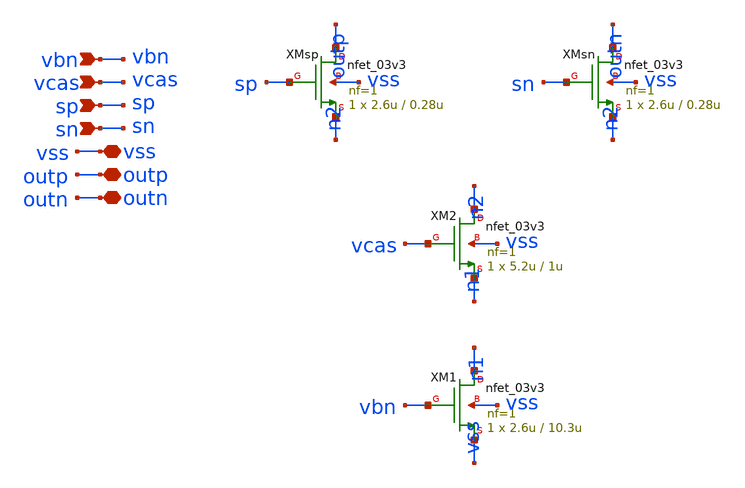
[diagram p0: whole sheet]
** sch_path: design/analog/unit_cell.sch
**.subckt unit_cell vbn vcas sp sn vss outp outn
*.ipin vbn
*.ipin vcas
*.ipin sp
*.ipin sn
*.iopin vss
*.iopin outp
*.iopin outn
XM1 n1 vbn vss vss nfet_03v3 L=10.3u W=2.6u nf=1 ad='int((nf+1)/2) * W/nf * 0.18u' as='int((nf+2)/2) * W/nf * 0.18u'
+ pd='2*int((nf+1)/2) * (W/nf + 0.18u)' ps='2*int((nf+2)/2) * (W/nf + 0.18u)' nrd='0.18u / W' nrs='0.18u / W'
+ sa=0 sb=0 sd=0 m=1
XM2 n2 vcas n1 vss nfet_03v3 L=1u W=5.2u nf=1 ad='int((nf+1)/2) * W/nf * 0.18u' as='int((nf+2)/2) * W/nf * 0.18u'
+ pd='2*int((nf+1)/2) * (W/nf + 0.18u)' ps='2*int((nf+2)/2) * (W/nf + 0.18u)' nrd='0.18u / W' nrs='0.18u / W'
+ sa=0 sb=0 sd=0 m=1
XMsp outp sp n2 vss nfet_03v3 L=0.28u W=2.6u nf=1 ad='int((nf+1)/2) * W/nf * 0.18u' as='int((nf+2)/2) * W/nf * 0.18u'
+ pd='2*int((nf+1)/2) * (W/nf + 0.18u)' ps='2*int((nf+2)/2) * (W/nf + 0.18u)' nrd='0.18u / W' nrs='0.18u / W'
+ sa=0 sb=0 sd=0 m=1
XMsn outn sn n2 vss nfet_03v3 L=0.28u W=2.6u nf=1 ad='int((nf+1)/2) * W/nf * 0.18u' as='int((nf+2)/2) * W/nf * 0.18u'
+ pd='2*int((nf+1)/2) * (W/nf + 0.18u)' ps='2*int((nf+2)/2) * (W/nf + 0.18u)' nrd='0.18u / W' nrs='0.18u / W'
+ sa=0 sb=0 sd=0 m=1
**.ends
.end
